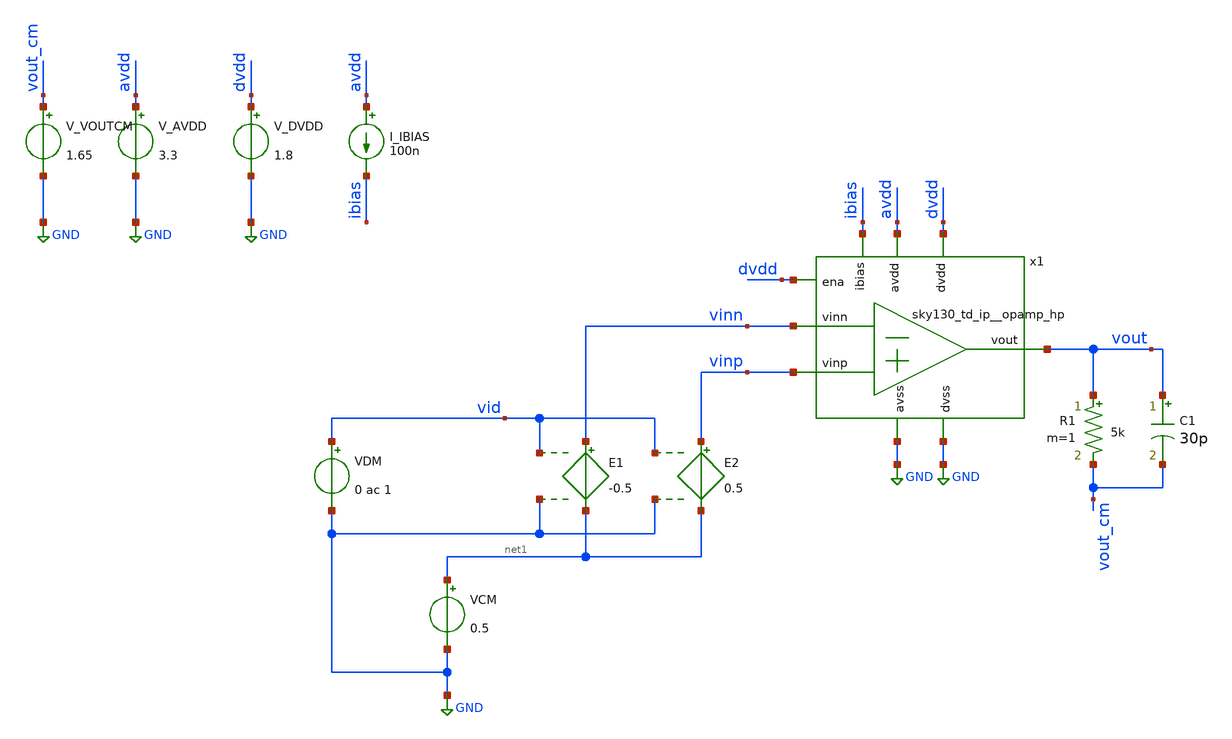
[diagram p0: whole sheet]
** sch_path: xschem/offset.sch
**.subckt offset
x1 avdd vout ibias vinn vinp GND dvdd GND dvdd sky130_td_ip__opamp_hp
V_AVDD avdd GND 3.3
.save i(v_avdd)
V_DVDD dvdd GND 1.8
.save i(v_dvdd)
I_IBIAS avdd ibias 100n
VCM net1 GND 0.5
R1 vout vout_cm 5k m=1
C1 vout vout_cm 30p m=1
V_VOUTCM vout_cm GND 1.65
.save i(v_voutcm)
E1 vinn net1 vid GND -0.5
VDM vid GND 0 ac 1
E2 vinp net1 vid GND 0.5
**** begin user architecture code


.save all

.control
save all

dc VDM 150u 200u 0.5u

run

let vout = v(vout)

meas DC input_offset_voltage WHEN vout=1.65


echo
echo ===================================
echo Differential-mode DC sweep results
echo - Input Offset voltage: $&input_offset_voltage
echo ===================================


plot vout

.endc




.lib /usr/local/share/pdk/sky130A/libs.tech/combined/sky130.lib.spice tt


**** end user architecture code
**.ends
.GLOBAL GND
.end
